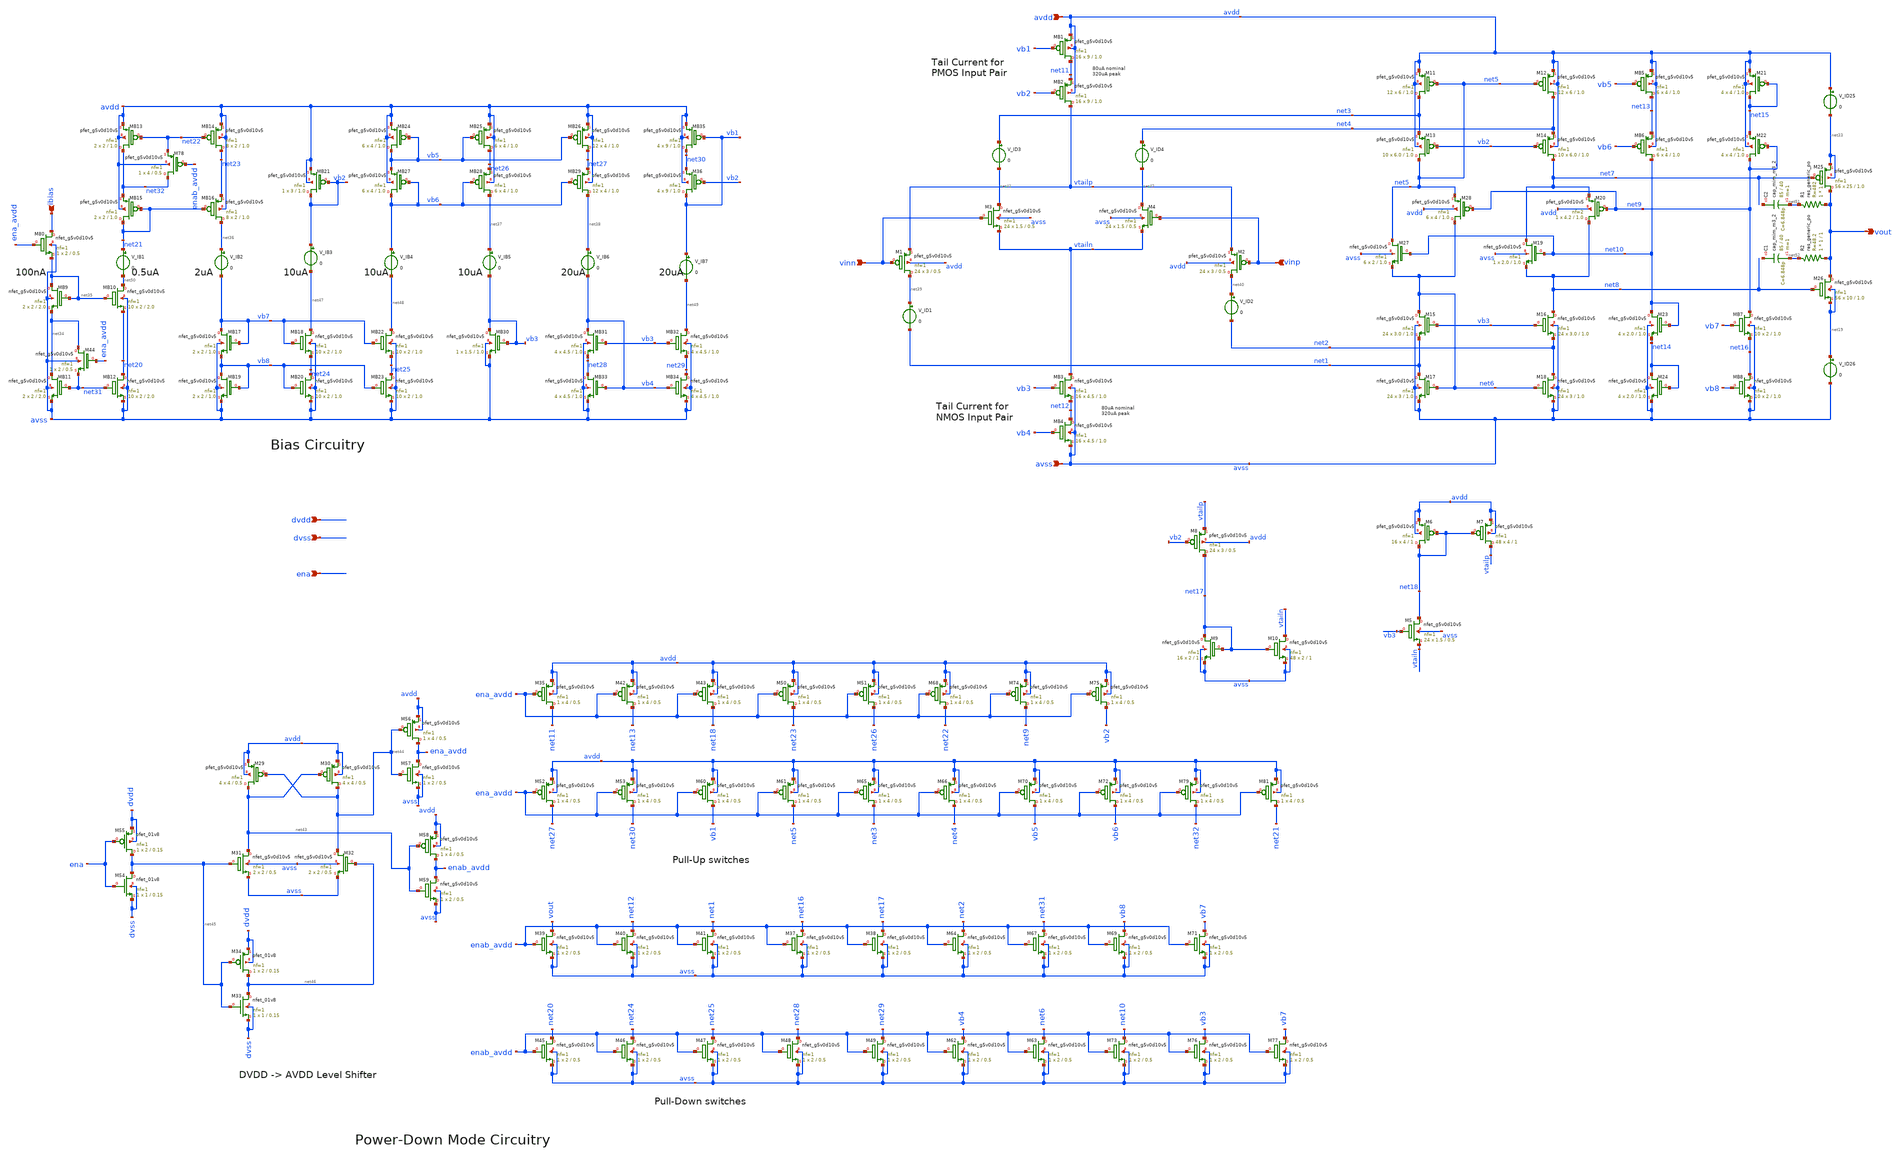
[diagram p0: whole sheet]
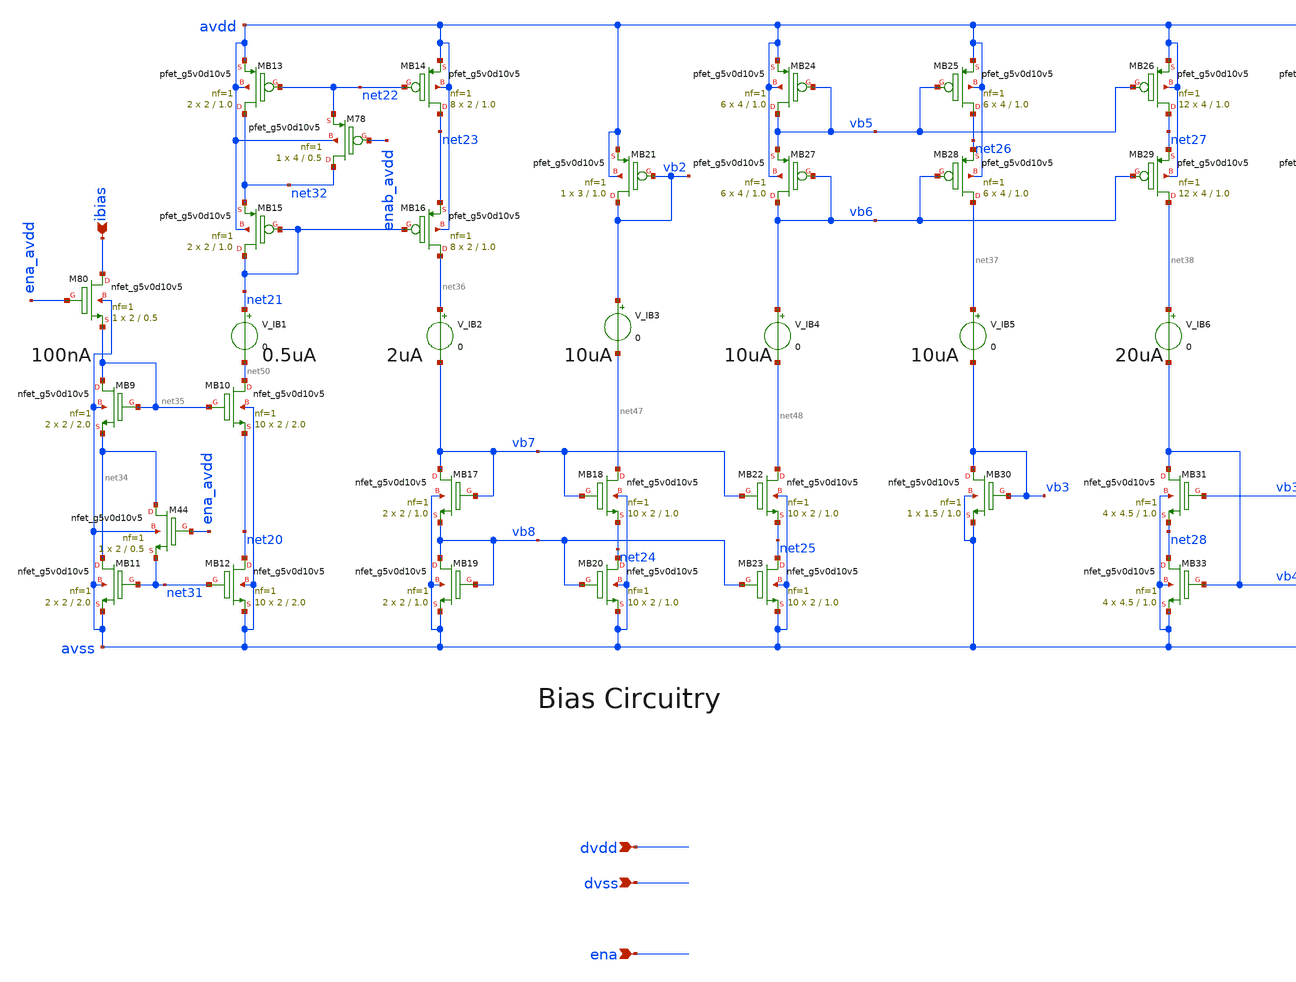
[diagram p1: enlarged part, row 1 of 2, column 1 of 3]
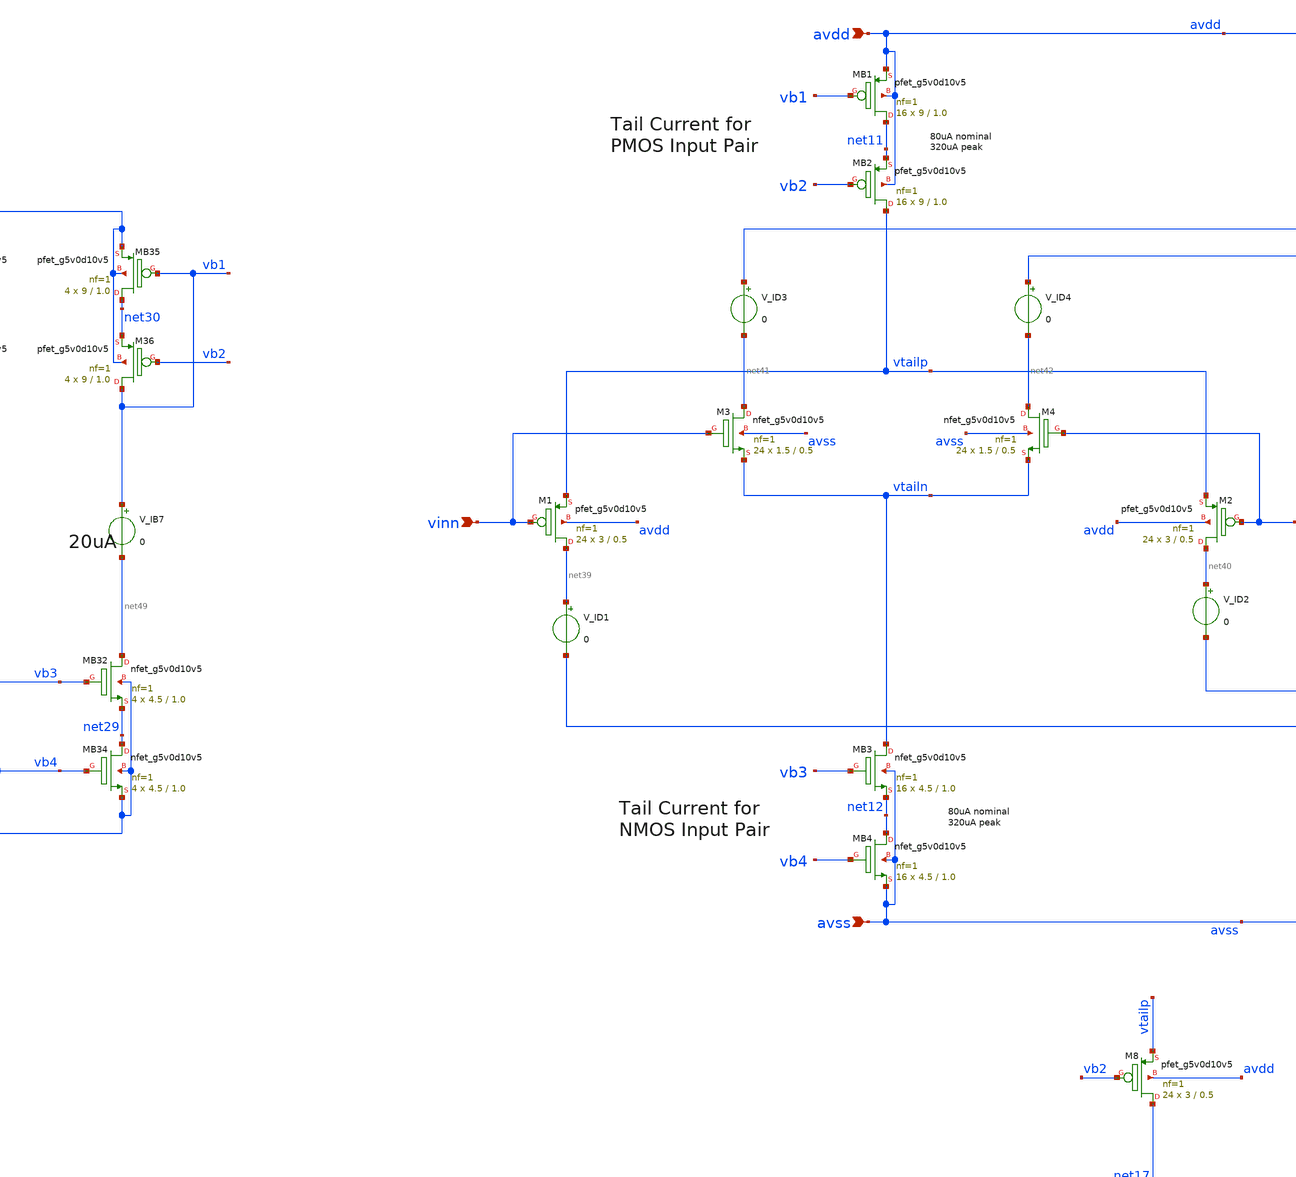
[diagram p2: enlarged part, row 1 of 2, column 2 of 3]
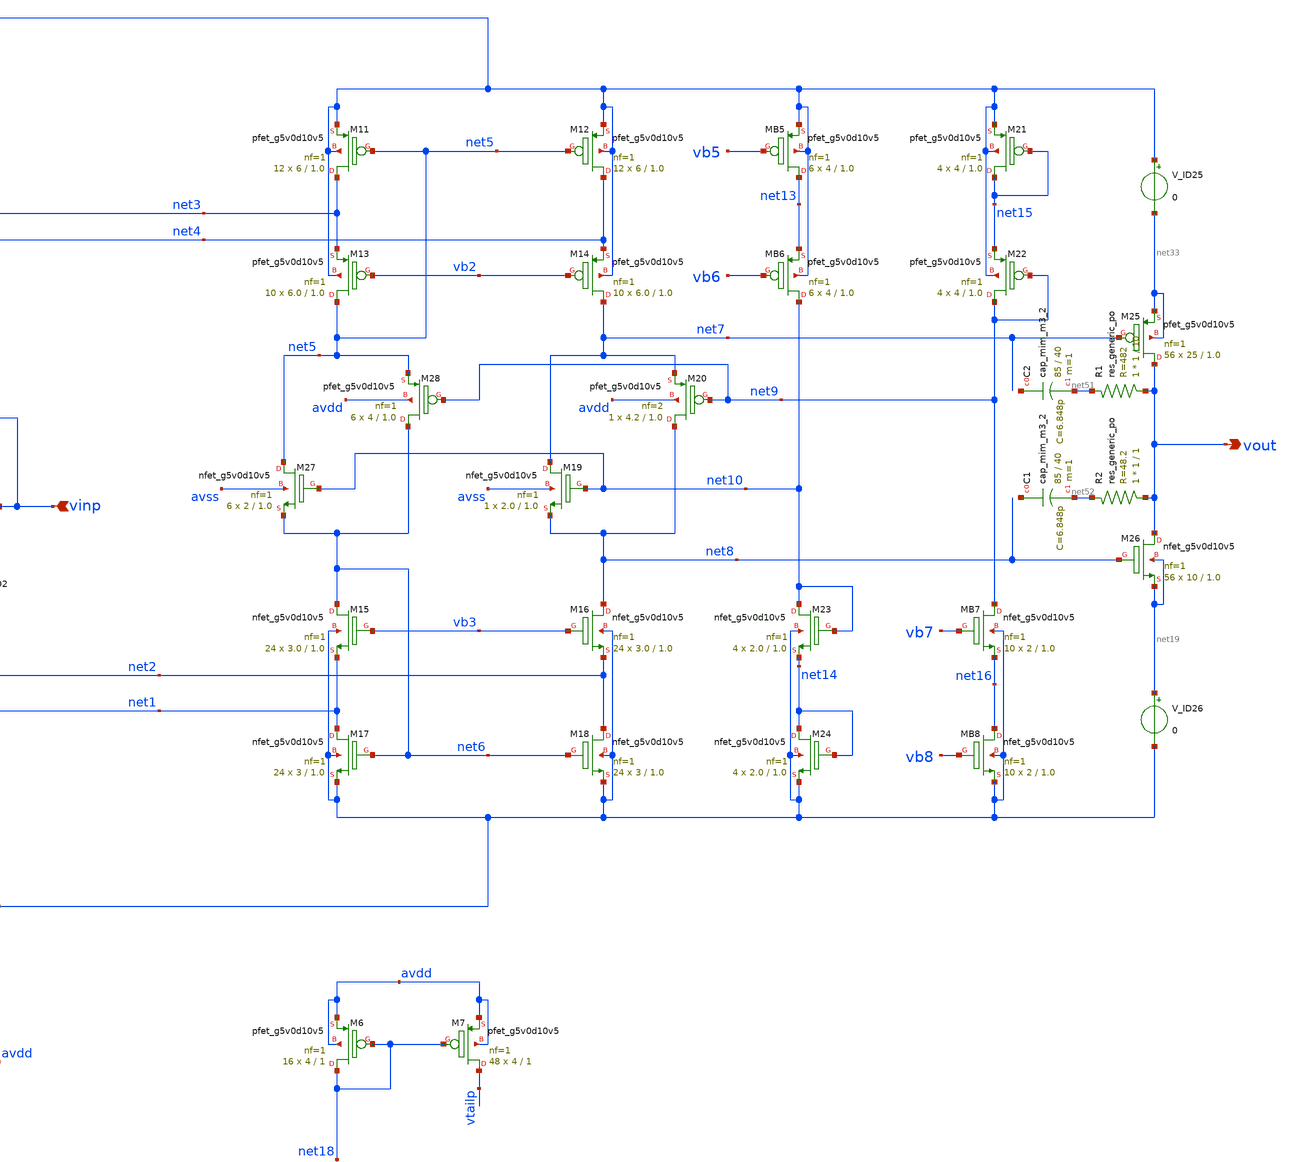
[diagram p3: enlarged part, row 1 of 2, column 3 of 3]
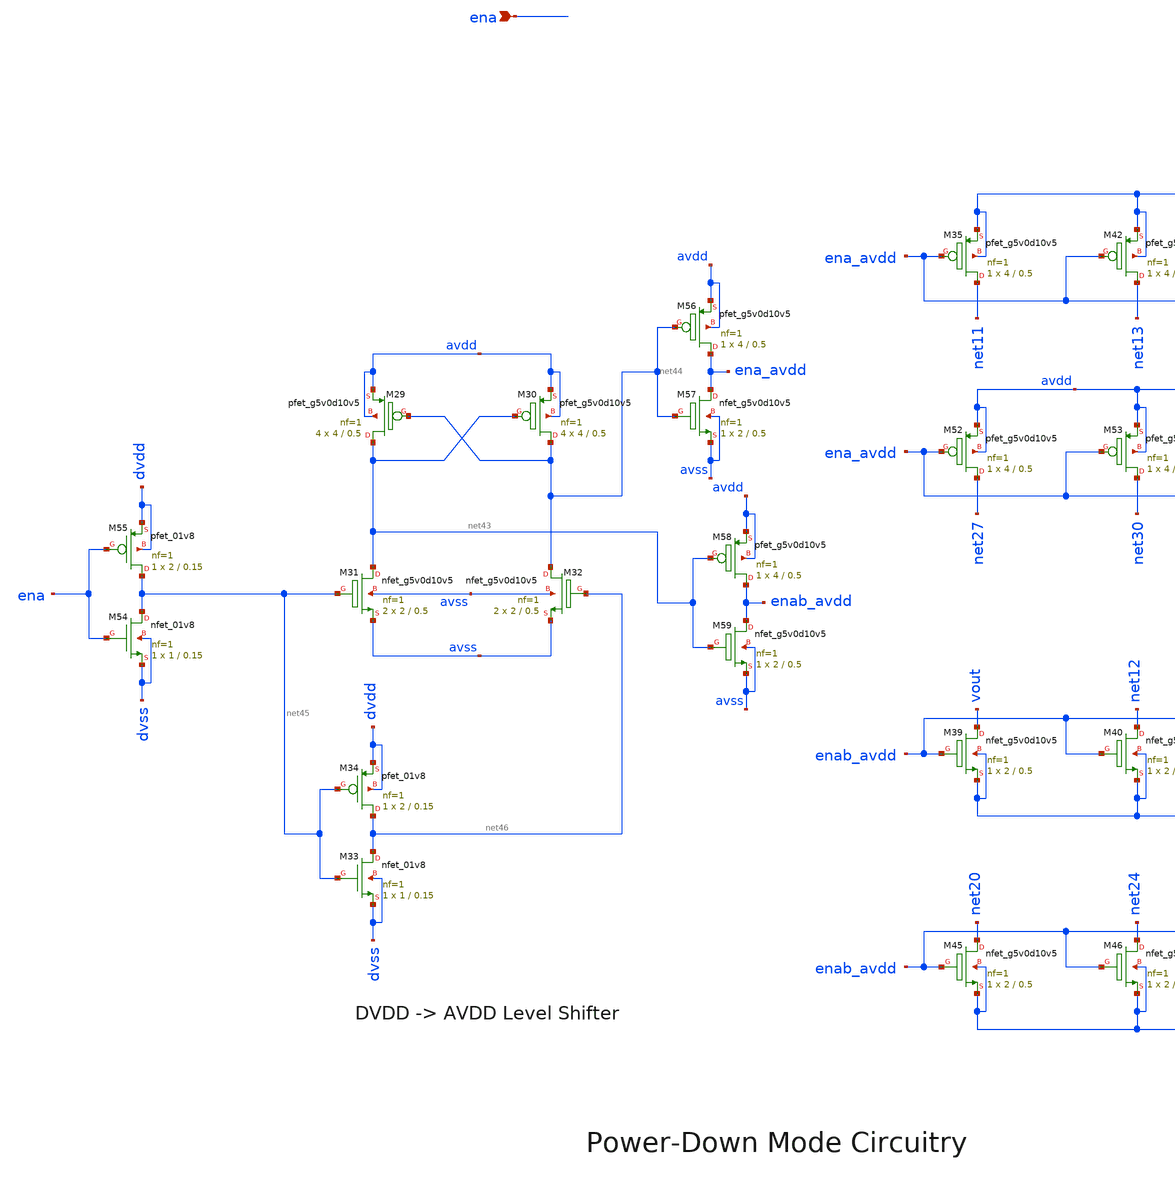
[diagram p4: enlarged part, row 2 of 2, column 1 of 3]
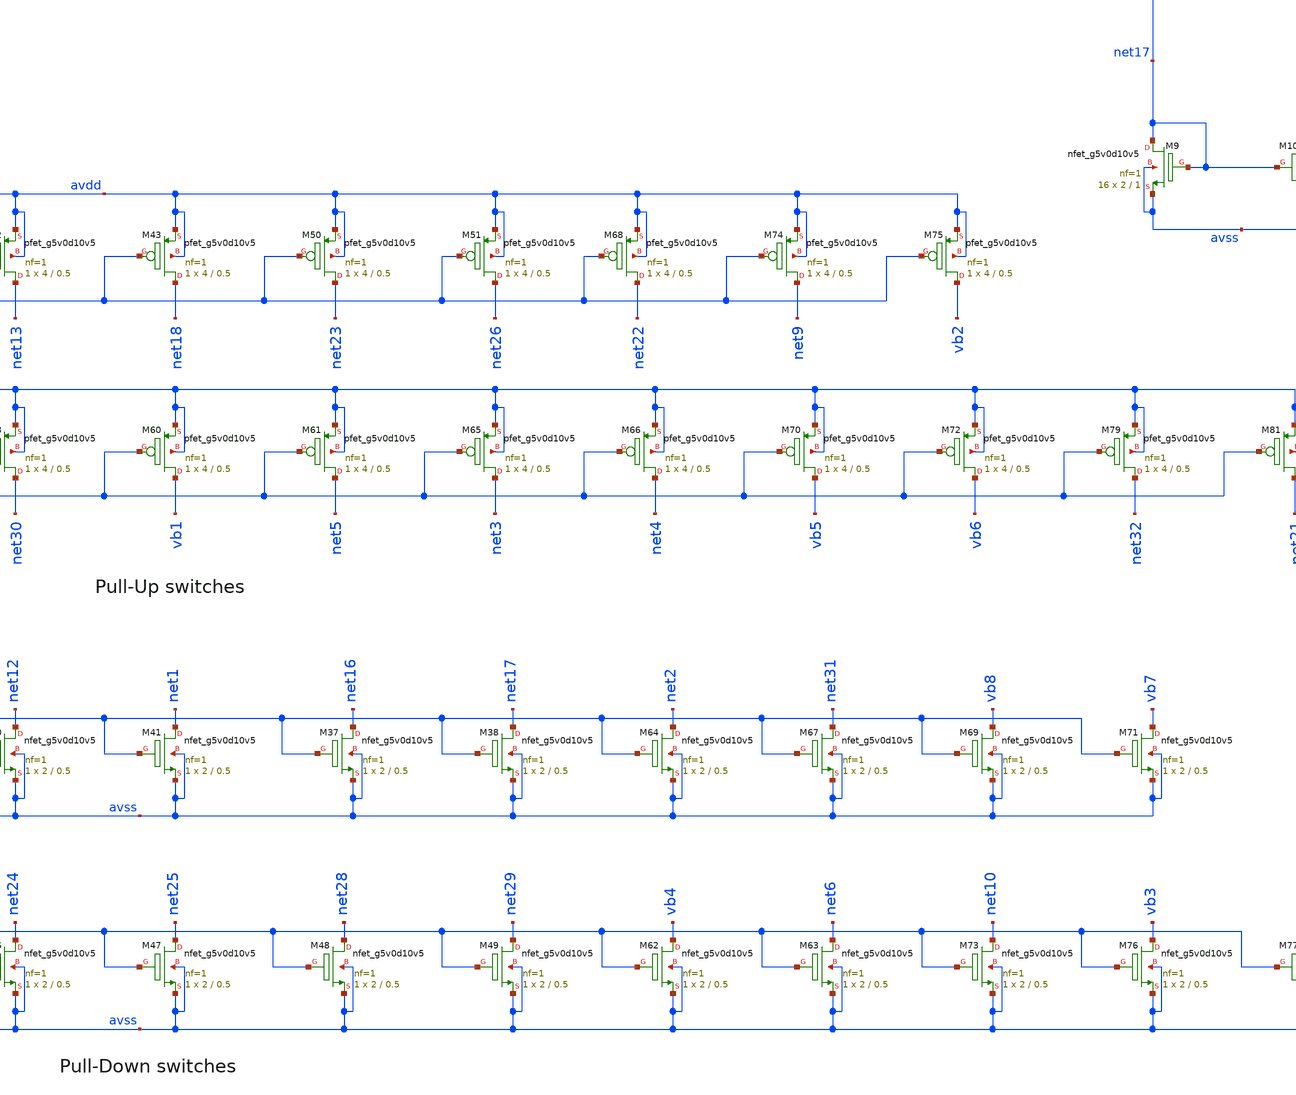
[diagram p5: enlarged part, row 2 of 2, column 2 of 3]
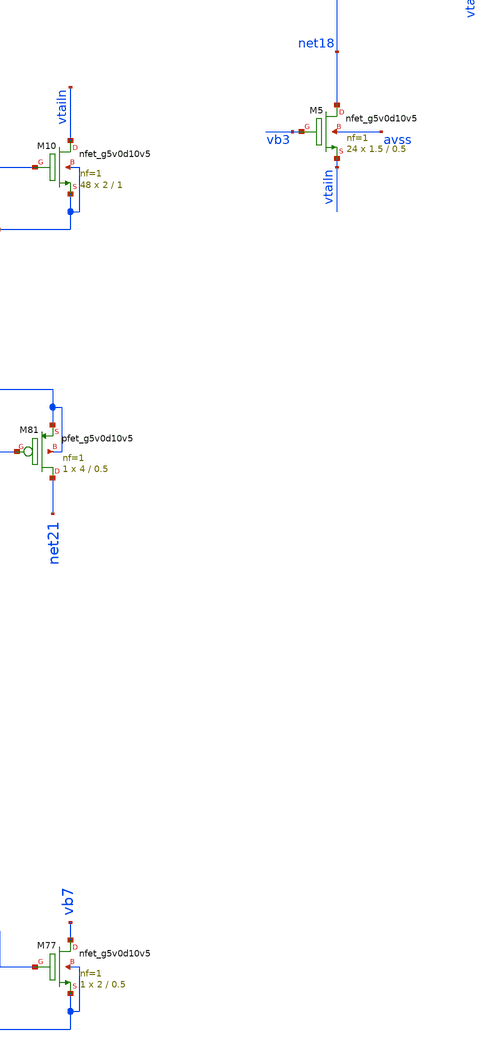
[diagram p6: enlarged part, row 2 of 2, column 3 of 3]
** sch_path: xschem/sky130_td_ip__opamp_hp.sch
**.subckt sky130_td_ip__opamp_hp vinn vinp vout ena ibias avss avdd dvdd dvss
*.ipin vinn
*.ipin vinp
*.opin vout
*.ipin ena
*.ipin ibias
*.ipin avss
*.ipin avdd
*.ipin dvdd
*.ipin dvss
XM3 net41 vinn vtailn avss sky130_fd_pr__nfet_g5v0d10v5 L=0.5 W=1.5 nf=1 ad='int((nf+1)/2) * W/nf * 0.29'
+ as='int((nf+2)/2) * W/nf * 0.29' pd='2*int((nf+1)/2) * (W/nf + 0.29)' ps='2*int((nf+2)/2) * (W/nf + 0.29)'
+ nrd='0.29 / W' nrs='0.29 / W' sa=0 sb=0 sd=0 mult=24 m=24
XM4 net42 vinp vtailn avss sky130_fd_pr__nfet_g5v0d10v5 L=0.5 W=1.5 nf=1 ad='int((nf+1)/2) * W/nf * 0.29'
+ as='int((nf+2)/2) * W/nf * 0.29' pd='2*int((nf+1)/2) * (W/nf + 0.29)' ps='2*int((nf+2)/2) * (W/nf + 0.29)'
+ nrd='0.29 / W' nrs='0.29 / W' sa=0 sb=0 sd=0 mult=24 m=24
XMB3 vtailn vb3 net12 avss sky130_fd_pr__nfet_g5v0d10v5 L=1.0 W=4.5 nf=1 ad='int((nf+1)/2) * W/nf * 0.29'
+ as='int((nf+2)/2) * W/nf * 0.29' pd='2*int((nf+1)/2) * (W/nf + 0.29)' ps='2*int((nf+2)/2) * (W/nf + 0.29)'
+ nrd='0.29 / W' nrs='0.29 / W' sa=0 sb=0 sd=0 mult=16 m=16
XMB4 net12 vb4 avss avss sky130_fd_pr__nfet_g5v0d10v5 L=1.0 W=4.5 nf=1 ad='int((nf+1)/2) * W/nf * 0.29'
+ as='int((nf+2)/2) * W/nf * 0.29' pd='2*int((nf+1)/2) * (W/nf + 0.29)' ps='2*int((nf+2)/2) * (W/nf + 0.29)'
+ nrd='0.29 / W' nrs='0.29 / W' sa=0 sb=0 sd=0 mult=16 m=16
XM1 net39 vinn vtailp avdd sky130_fd_pr__pfet_g5v0d10v5 L=0.5 W=3 nf=1 ad='int((nf+1)/2) * W/nf * 0.29'
+ as='int((nf+2)/2) * W/nf * 0.29' pd='2*int((nf+1)/2) * (W/nf + 0.29)' ps='2*int((nf+2)/2) * (W/nf + 0.29)'
+ nrd='0.29 / W' nrs='0.29 / W' sa=0 sb=0 sd=0 mult=24 m=24
XM2 net40 vinp vtailp avdd sky130_fd_pr__pfet_g5v0d10v5 L=0.5 W=3 nf=1 ad='int((nf+1)/2) * W/nf * 0.29'
+ as='int((nf+2)/2) * W/nf * 0.29' pd='2*int((nf+1)/2) * (W/nf + 0.29)' ps='2*int((nf+2)/2) * (W/nf + 0.29)'
+ nrd='0.29 / W' nrs='0.29 / W' sa=0 sb=0 sd=0 mult=24 m=24
XMB2 vtailp vb2 net11 avdd sky130_fd_pr__pfet_g5v0d10v5 L=1.0 W=9 nf=1 ad='int((nf+1)/2) * W/nf * 0.29'
+ as='int((nf+2)/2) * W/nf * 0.29' pd='2*int((nf+1)/2) * (W/nf + 0.29)' ps='2*int((nf+2)/2) * (W/nf + 0.29)'
+ nrd='0.29 / W' nrs='0.29 / W' sa=0 sb=0 sd=0 mult=16 m=16
XMB1 net11 vb1 avdd avdd sky130_fd_pr__pfet_g5v0d10v5 L=1.0 W=9 nf=1 ad='int((nf+1)/2) * W/nf * 0.29'
+ as='int((nf+2)/2) * W/nf * 0.29' pd='2*int((nf+1)/2) * (W/nf + 0.29)' ps='2*int((nf+2)/2) * (W/nf + 0.29)'
+ nrd='0.29 / W' nrs='0.29 / W' sa=0 sb=0 sd=0 mult=16 m=16
XM12 net4 net5 avdd avdd sky130_fd_pr__pfet_g5v0d10v5 L=1.0 W=6 nf=1 ad='int((nf+1)/2) * W/nf * 0.29'
+ as='int((nf+2)/2) * W/nf * 0.29' pd='2*int((nf+1)/2) * (W/nf + 0.29)' ps='2*int((nf+2)/2) * (W/nf + 0.29)'
+ nrd='0.29 / W' nrs='0.29 / W' sa=0 sb=0 sd=0 mult=12 m=12
XM11 net3 net5 avdd avdd sky130_fd_pr__pfet_g5v0d10v5 L=1.0 W=6 nf=1 ad='int((nf+1)/2) * W/nf * 0.29'
+ as='int((nf+2)/2) * W/nf * 0.29' pd='2*int((nf+1)/2) * (W/nf + 0.29)' ps='2*int((nf+2)/2) * (W/nf + 0.29)'
+ nrd='0.29 / W' nrs='0.29 / W' sa=0 sb=0 sd=0 mult=12 m=12
XM14 net7 vb2 net4 avdd sky130_fd_pr__pfet_g5v0d10v5 L=1.0 W=6.0 nf=1 ad='int((nf+1)/2) * W/nf * 0.29'
+ as='int((nf+2)/2) * W/nf * 0.29' pd='2*int((nf+1)/2) * (W/nf + 0.29)' ps='2*int((nf+2)/2) * (W/nf + 0.29)'
+ nrd='0.29 / W' nrs='0.29 / W' sa=0 sb=0 sd=0 mult=10 m=10
XM13 net5 vb2 net3 avdd sky130_fd_pr__pfet_g5v0d10v5 L=1.0 W=6.0 nf=1 ad='int((nf+1)/2) * W/nf * 0.29'
+ as='int((nf+2)/2) * W/nf * 0.29' pd='2*int((nf+1)/2) * (W/nf + 0.29)' ps='2*int((nf+2)/2) * (W/nf + 0.29)'
+ nrd='0.29 / W' nrs='0.29 / W' sa=0 sb=0 sd=0 mult=10 m=10
XM18 net2 net6 avss avss sky130_fd_pr__nfet_g5v0d10v5 L=1.0 W=3 nf=1 ad='int((nf+1)/2) * W/nf * 0.29'
+ as='int((nf+2)/2) * W/nf * 0.29' pd='2*int((nf+1)/2) * (W/nf + 0.29)' ps='2*int((nf+2)/2) * (W/nf + 0.29)'
+ nrd='0.29 / W' nrs='0.29 / W' sa=0 sb=0 sd=0 mult=24 m=24
XM16 net8 vb3 net2 avss sky130_fd_pr__nfet_g5v0d10v5 L=1.0 W=3.0 nf=1 ad='int((nf+1)/2) * W/nf * 0.29'
+ as='int((nf+2)/2) * W/nf * 0.29' pd='2*int((nf+1)/2) * (W/nf + 0.29)' ps='2*int((nf+2)/2) * (W/nf + 0.29)'
+ nrd='0.29 / W' nrs='0.29 / W' sa=0 sb=0 sd=0 mult=24 m=24
XM17 net1 net6 avss avss sky130_fd_pr__nfet_g5v0d10v5 L=1.0 W=3 nf=1 ad='int((nf+1)/2) * W/nf * 0.29'
+ as='int((nf+2)/2) * W/nf * 0.29' pd='2*int((nf+1)/2) * (W/nf + 0.29)' ps='2*int((nf+2)/2) * (W/nf + 0.29)'
+ nrd='0.29 / W' nrs='0.29 / W' sa=0 sb=0 sd=0 mult=24 m=24
XM15 net6 vb3 net1 avss sky130_fd_pr__nfet_g5v0d10v5 L=1.0 W=3.0 nf=1 ad='int((nf+1)/2) * W/nf * 0.29'
+ as='int((nf+2)/2) * W/nf * 0.29' pd='2*int((nf+1)/2) * (W/nf + 0.29)' ps='2*int((nf+2)/2) * (W/nf + 0.29)'
+ nrd='0.29 / W' nrs='0.29 / W' sa=0 sb=0 sd=0 mult=24 m=24
XM28 net6 net9 net5 avdd sky130_fd_pr__pfet_g5v0d10v5 L=1.0 W=4 nf=1 ad='int((nf+1)/2) * W/nf * 0.29'
+ as='int((nf+2)/2) * W/nf * 0.29' pd='2*int((nf+1)/2) * (W/nf + 0.29)' ps='2*int((nf+2)/2) * (W/nf + 0.29)'
+ nrd='0.29 / W' nrs='0.29 / W' sa=0 sb=0 sd=0 mult=6 m=6
XM27 net5 net10 net6 avss sky130_fd_pr__nfet_g5v0d10v5 L=1.0 W=2 nf=1 ad='int((nf+1)/2) * W/nf * 0.29'
+ as='int((nf+2)/2) * W/nf * 0.29' pd='2*int((nf+1)/2) * (W/nf + 0.29)' ps='2*int((nf+2)/2) * (W/nf + 0.29)'
+ nrd='0.29 / W' nrs='0.29 / W' sa=0 sb=0 sd=0 mult=6 m=6
XM20 net8 net9 net7 avdd sky130_fd_pr__pfet_g5v0d10v5 L=1.0 W=4.2 nf=2 ad='int((nf+1)/2) * W/nf * 0.29'
+ as='int((nf+2)/2) * W/nf * 0.29' pd='2*int((nf+1)/2) * (W/nf + 0.29)' ps='2*int((nf+2)/2) * (W/nf + 0.29)'
+ nrd='0.29 / W' nrs='0.29 / W' sa=0 sb=0 sd=0 mult=1 m=1
XM19 net7 net10 net8 avss sky130_fd_pr__nfet_g5v0d10v5 L=1.0 W=2.0 nf=1 ad='int((nf+1)/2) * W/nf * 0.29'
+ as='int((nf+2)/2) * W/nf * 0.29' pd='2*int((nf+1)/2) * (W/nf + 0.29)' ps='2*int((nf+2)/2) * (W/nf + 0.29)'
+ nrd='0.29 / W' nrs='0.29 / W' sa=0 sb=0 sd=0 mult=1 m=1
XM26 vout net8 net19 net19 sky130_fd_pr__nfet_g5v0d10v5 L=1.0 W=10 nf=1 ad='int((nf+1)/2) * W/nf * 0.29'
+ as='int((nf+2)/2) * W/nf * 0.29' pd='2*int((nf+1)/2) * (W/nf + 0.29)' ps='2*int((nf+2)/2) * (W/nf + 0.29)'
+ nrd='0.29 / W' nrs='0.29 / W' sa=0 sb=0 sd=0 mult=56 m=56
XM25 vout net7 net33 net33 sky130_fd_pr__pfet_g5v0d10v5 L=1.0 W=25 nf=1 ad='int((nf+1)/2) * W/nf * 0.29'
+ as='int((nf+2)/2) * W/nf * 0.29' pd='2*int((nf+1)/2) * (W/nf + 0.29)' ps='2*int((nf+2)/2) * (W/nf + 0.29)'
+ nrd='0.29 / W' nrs='0.29 / W' sa=0 sb=0 sd=0 mult=56 m=56
XMB9 net35 net35 net34 avss sky130_fd_pr__nfet_g5v0d10v5 L=2.0 W=2 nf=1 ad='int((nf+1)/2) * W/nf * 0.29'
+ as='int((nf+2)/2) * W/nf * 0.29' pd='2*int((nf+1)/2) * (W/nf + 0.29)' ps='2*int((nf+2)/2) * (W/nf + 0.29)'
+ nrd='0.29 / W' nrs='0.29 / W' sa=0 sb=0 sd=0 mult=2 m=2
XMB11 net34 net31 avss avss sky130_fd_pr__nfet_g5v0d10v5 L=2.0 W=2 nf=1 ad='int((nf+1)/2) * W/nf * 0.29'
+ as='int((nf+2)/2) * W/nf * 0.29' pd='2*int((nf+1)/2) * (W/nf + 0.29)' ps='2*int((nf+2)/2) * (W/nf + 0.29)'
+ nrd='0.29 / W' nrs='0.29 / W' sa=0 sb=0 sd=0 mult=2 m=2
XMB10 net50 net35 net20 avss sky130_fd_pr__nfet_g5v0d10v5 L=2.0 W=2 nf=1 ad='int((nf+1)/2) * W/nf * 0.29'
+ as='int((nf+2)/2) * W/nf * 0.29' pd='2*int((nf+1)/2) * (W/nf + 0.29)' ps='2*int((nf+2)/2) * (W/nf + 0.29)'
+ nrd='0.29 / W' nrs='0.29 / W' sa=0 sb=0 sd=0 mult=10 m=10
XMB12 net20 net31 avss avss sky130_fd_pr__nfet_g5v0d10v5 L=2.0 W=2 nf=1 ad='int((nf+1)/2) * W/nf * 0.29'
+ as='int((nf+2)/2) * W/nf * 0.29' pd='2*int((nf+1)/2) * (W/nf + 0.29)' ps='2*int((nf+2)/2) * (W/nf + 0.29)'
+ nrd='0.29 / W' nrs='0.29 / W' sa=0 sb=0 sd=0 mult=10 m=10
XMB15 net21 net21 net32 avdd sky130_fd_pr__pfet_g5v0d10v5 L=1.0 W=2 nf=1 ad='int((nf+1)/2) * W/nf * 0.29'
+ as='int((nf+2)/2) * W/nf * 0.29' pd='2*int((nf+1)/2) * (W/nf + 0.29)' ps='2*int((nf+2)/2) * (W/nf + 0.29)'
+ nrd='0.29 / W' nrs='0.29 / W' sa=0 sb=0 sd=0 mult=2 m=2
XMB13 net32 net22 avdd avdd sky130_fd_pr__pfet_g5v0d10v5 L=1.0 W=2 nf=1 ad='int((nf+1)/2) * W/nf * 0.29'
+ as='int((nf+2)/2) * W/nf * 0.29' pd='2*int((nf+1)/2) * (W/nf + 0.29)' ps='2*int((nf+2)/2) * (W/nf + 0.29)'
+ nrd='0.29 / W' nrs='0.29 / W' sa=0 sb=0 sd=0 mult=2 m=2
XMB16 net36 net21 net23 avdd sky130_fd_pr__pfet_g5v0d10v5 L=1.0 W=2 nf=1 ad='int((nf+1)/2) * W/nf * 0.29'
+ as='int((nf+2)/2) * W/nf * 0.29' pd='2*int((nf+1)/2) * (W/nf + 0.29)' ps='2*int((nf+2)/2) * (W/nf + 0.29)'
+ nrd='0.29 / W' nrs='0.29 / W' sa=0 sb=0 sd=0 mult=8 m=8
XMB14 net23 net22 avdd avdd sky130_fd_pr__pfet_g5v0d10v5 L=1.0 W=2 nf=1 ad='int((nf+1)/2) * W/nf * 0.29'
+ as='int((nf+2)/2) * W/nf * 0.29' pd='2*int((nf+1)/2) * (W/nf + 0.29)' ps='2*int((nf+2)/2) * (W/nf + 0.29)'
+ nrd='0.29 / W' nrs='0.29 / W' sa=0 sb=0 sd=0 mult=8 m=8
XMB17 vb7 vb7 vb8 avss sky130_fd_pr__nfet_g5v0d10v5 L=1.0 W=2 nf=1 ad='int((nf+1)/2) * W/nf * 0.29' as='int((nf+2)/2) * W/nf * 0.29'
+ pd='2*int((nf+1)/2) * (W/nf + 0.29)' ps='2*int((nf+2)/2) * (W/nf + 0.29)' nrd='0.29 / W' nrs='0.29 / W'
+ sa=0 sb=0 sd=0 mult=2 m=2
XMB19 vb8 vb8 avss avss sky130_fd_pr__nfet_g5v0d10v5 L=1.0 W=2 nf=1 ad='int((nf+1)/2) * W/nf * 0.29'
+ as='int((nf+2)/2) * W/nf * 0.29' pd='2*int((nf+1)/2) * (W/nf + 0.29)' ps='2*int((nf+2)/2) * (W/nf + 0.29)'
+ nrd='0.29 / W' nrs='0.29 / W' sa=0 sb=0 sd=0 mult=2 m=2
XMB18 net47 vb7 net24 avss sky130_fd_pr__nfet_g5v0d10v5 L=1.0 W=2 nf=1 ad='int((nf+1)/2) * W/nf * 0.29'
+ as='int((nf+2)/2) * W/nf * 0.29' pd='2*int((nf+1)/2) * (W/nf + 0.29)' ps='2*int((nf+2)/2) * (W/nf + 0.29)'
+ nrd='0.29 / W' nrs='0.29 / W' sa=0 sb=0 sd=0 mult=10 m=10
XMB20 net24 vb8 avss avss sky130_fd_pr__nfet_g5v0d10v5 L=1.0 W=2 nf=1 ad='int((nf+1)/2) * W/nf * 0.29'
+ as='int((nf+2)/2) * W/nf * 0.29' pd='2*int((nf+1)/2) * (W/nf + 0.29)' ps='2*int((nf+2)/2) * (W/nf + 0.29)'
+ nrd='0.29 / W' nrs='0.29 / W' sa=0 sb=0 sd=0 mult=10 m=10
XMB22 net48 vb7 net25 avss sky130_fd_pr__nfet_g5v0d10v5 L=1.0 W=2 nf=1 ad='int((nf+1)/2) * W/nf * 0.29'
+ as='int((nf+2)/2) * W/nf * 0.29' pd='2*int((nf+1)/2) * (W/nf + 0.29)' ps='2*int((nf+2)/2) * (W/nf + 0.29)'
+ nrd='0.29 / W' nrs='0.29 / W' sa=0 sb=0 sd=0 mult=10 m=10
XMB23 net25 vb8 avss avss sky130_fd_pr__nfet_g5v0d10v5 L=1.0 W=2 nf=1 ad='int((nf+1)/2) * W/nf * 0.29'
+ as='int((nf+2)/2) * W/nf * 0.29' pd='2*int((nf+1)/2) * (W/nf + 0.29)' ps='2*int((nf+2)/2) * (W/nf + 0.29)'
+ nrd='0.29 / W' nrs='0.29 / W' sa=0 sb=0 sd=0 mult=10 m=10
XMB21 vb2 vb2 avdd avdd sky130_fd_pr__pfet_g5v0d10v5 L=1.0 W=3 nf=1 ad='int((nf+1)/2) * W/nf * 0.29'
+ as='int((nf+2)/2) * W/nf * 0.29' pd='2*int((nf+1)/2) * (W/nf + 0.29)' ps='2*int((nf+2)/2) * (W/nf + 0.29)'
+ nrd='0.29 / W' nrs='0.29 / W' sa=0 sb=0 sd=0 mult=1 m=1
XMB27 vb6 vb6 vb5 avdd sky130_fd_pr__pfet_g5v0d10v5 L=1.0 W=4 nf=1 ad='int((nf+1)/2) * W/nf * 0.29' as='int((nf+2)/2) * W/nf * 0.29'
+ pd='2*int((nf+1)/2) * (W/nf + 0.29)' ps='2*int((nf+2)/2) * (W/nf + 0.29)' nrd='0.29 / W' nrs='0.29 / W'
+ sa=0 sb=0 sd=0 mult=6 m=6
XMB24 vb5 vb5 avdd avdd sky130_fd_pr__pfet_g5v0d10v5 L=1.0 W=4 nf=1 ad='int((nf+1)/2) * W/nf * 0.29'
+ as='int((nf+2)/2) * W/nf * 0.29' pd='2*int((nf+1)/2) * (W/nf + 0.29)' ps='2*int((nf+2)/2) * (W/nf + 0.29)'
+ nrd='0.29 / W' nrs='0.29 / W' sa=0 sb=0 sd=0 mult=6 m=6
XMB28 net37 vb6 net26 avdd sky130_fd_pr__pfet_g5v0d10v5 L=1.0 W=4 nf=1 ad='int((nf+1)/2) * W/nf * 0.29'
+ as='int((nf+2)/2) * W/nf * 0.29' pd='2*int((nf+1)/2) * (W/nf + 0.29)' ps='2*int((nf+2)/2) * (W/nf + 0.29)'
+ nrd='0.29 / W' nrs='0.29 / W' sa=0 sb=0 sd=0 mult=6 m=6
XMB25 net26 vb5 avdd avdd sky130_fd_pr__pfet_g5v0d10v5 L=1.0 W=4 nf=1 ad='int((nf+1)/2) * W/nf * 0.29'
+ as='int((nf+2)/2) * W/nf * 0.29' pd='2*int((nf+1)/2) * (W/nf + 0.29)' ps='2*int((nf+2)/2) * (W/nf + 0.29)'
+ nrd='0.29 / W' nrs='0.29 / W' sa=0 sb=0 sd=0 mult=6 m=6
XMB29 net38 vb6 net27 avdd sky130_fd_pr__pfet_g5v0d10v5 L=1.0 W=4 nf=1 ad='int((nf+1)/2) * W/nf * 0.29'
+ as='int((nf+2)/2) * W/nf * 0.29' pd='2*int((nf+1)/2) * (W/nf + 0.29)' ps='2*int((nf+2)/2) * (W/nf + 0.29)'
+ nrd='0.29 / W' nrs='0.29 / W' sa=0 sb=0 sd=0 mult=12 m=12
XMB26 net27 vb5 avdd avdd sky130_fd_pr__pfet_g5v0d10v5 L=1.0 W=4 nf=1 ad='int((nf+1)/2) * W/nf * 0.29'
+ as='int((nf+2)/2) * W/nf * 0.29' pd='2*int((nf+1)/2) * (W/nf + 0.29)' ps='2*int((nf+2)/2) * (W/nf + 0.29)'
+ nrd='0.29 / W' nrs='0.29 / W' sa=0 sb=0 sd=0 mult=12 m=12
XMB30 vb3 vb3 avss avss sky130_fd_pr__nfet_g5v0d10v5 L=1.0 W=1.5 nf=1 ad='int((nf+1)/2) * W/nf * 0.29'
+ as='int((nf+2)/2) * W/nf * 0.29' pd='2*int((nf+1)/2) * (W/nf + 0.29)' ps='2*int((nf+2)/2) * (W/nf + 0.29)'
+ nrd='0.29 / W' nrs='0.29 / W' sa=0 sb=0 sd=0 mult=1 m=1
XMB31 vb4 vb3 net28 avss sky130_fd_pr__nfet_g5v0d10v5 L=1.0 W=4.5 nf=1 ad='int((nf+1)/2) * W/nf * 0.29'
+ as='int((nf+2)/2) * W/nf * 0.29' pd='2*int((nf+1)/2) * (W/nf + 0.29)' ps='2*int((nf+2)/2) * (W/nf + 0.29)'
+ nrd='0.29 / W' nrs='0.29 / W' sa=0 sb=0 sd=0 mult=4 m=4
XMB33 net28 vb4 avss avss sky130_fd_pr__nfet_g5v0d10v5 L=1.0 W=4.5 nf=1 ad='int((nf+1)/2) * W/nf * 0.29'
+ as='int((nf+2)/2) * W/nf * 0.29' pd='2*int((nf+1)/2) * (W/nf + 0.29)' ps='2*int((nf+2)/2) * (W/nf + 0.29)'
+ nrd='0.29 / W' nrs='0.29 / W' sa=0 sb=0 sd=0 mult=4 m=4
XMB32 net49 vb3 net29 avss sky130_fd_pr__nfet_g5v0d10v5 L=1.0 W=4.5 nf=1 ad='int((nf+1)/2) * W/nf * 0.29'
+ as='int((nf+2)/2) * W/nf * 0.29' pd='2*int((nf+1)/2) * (W/nf + 0.29)' ps='2*int((nf+2)/2) * (W/nf + 0.29)'
+ nrd='0.29 / W' nrs='0.29 / W' sa=0 sb=0 sd=0 mult=4 m=4
XMB34 net29 vb4 avss avss sky130_fd_pr__nfet_g5v0d10v5 L=1.0 W=4.5 nf=1 ad='int((nf+1)/2) * W/nf * 0.29'
+ as='int((nf+2)/2) * W/nf * 0.29' pd='2*int((nf+1)/2) * (W/nf + 0.29)' ps='2*int((nf+2)/2) * (W/nf + 0.29)'
+ nrd='0.29 / W' nrs='0.29 / W' sa=0 sb=0 sd=0 mult=4 m=4
XM36 vb1 vb2 net30 avdd sky130_fd_pr__pfet_g5v0d10v5 L=1.0 W=9 nf=1 ad='int((nf+1)/2) * W/nf * 0.29'
+ as='int((nf+2)/2) * W/nf * 0.29' pd='2*int((nf+1)/2) * (W/nf + 0.29)' ps='2*int((nf+2)/2) * (W/nf + 0.29)'
+ nrd='0.29 / W' nrs='0.29 / W' sa=0 sb=0 sd=0 mult=4 m=4
XMB35 net30 vb1 avdd avdd sky130_fd_pr__pfet_g5v0d10v5 L=1.0 W=9 nf=1 ad='int((nf+1)/2) * W/nf * 0.29'
+ as='int((nf+2)/2) * W/nf * 0.29' pd='2*int((nf+1)/2) * (W/nf + 0.29)' ps='2*int((nf+2)/2) * (W/nf + 0.29)'
+ nrd='0.29 / W' nrs='0.29 / W' sa=0 sb=0 sd=0 mult=4 m=4
XM24 net14 net14 avss avss sky130_fd_pr__nfet_g5v0d10v5 L=1.0 W=2.0 nf=1 ad='int((nf+1)/2) * W/nf * 0.29'
+ as='int((nf+2)/2) * W/nf * 0.29' pd='2*int((nf+1)/2) * (W/nf + 0.29)' ps='2*int((nf+2)/2) * (W/nf + 0.29)'
+ nrd='0.29 / W' nrs='0.29 / W' sa=0 sb=0 sd=0 mult=4 m=4
XM23 net10 net10 net14 avss sky130_fd_pr__nfet_g5v0d10v5 L=1.0 W=2.0 nf=1 ad='int((nf+1)/2) * W/nf * 0.29'
+ as='int((nf+2)/2) * W/nf * 0.29' pd='2*int((nf+1)/2) * (W/nf + 0.29)' ps='2*int((nf+2)/2) * (W/nf + 0.29)'
+ nrd='0.29 / W' nrs='0.29 / W' sa=0 sb=0 sd=0 mult=4 m=4
XMB5 net13 vb5 avdd avdd sky130_fd_pr__pfet_g5v0d10v5 L=1.0 W=4 nf=1 ad='int((nf+1)/2) * W/nf * 0.29'
+ as='int((nf+2)/2) * W/nf * 0.29' pd='2*int((nf+1)/2) * (W/nf + 0.29)' ps='2*int((nf+2)/2) * (W/nf + 0.29)'
+ nrd='0.29 / W' nrs='0.29 / W' sa=0 sb=0 sd=0 mult=6 m=6
XMB6 net10 vb6 net13 avdd sky130_fd_pr__pfet_g5v0d10v5 L=1.0 W=4 nf=1 ad='int((nf+1)/2) * W/nf * 0.29'
+ as='int((nf+2)/2) * W/nf * 0.29' pd='2*int((nf+1)/2) * (W/nf + 0.29)' ps='2*int((nf+2)/2) * (W/nf + 0.29)'
+ nrd='0.29 / W' nrs='0.29 / W' sa=0 sb=0 sd=0 mult=6 m=6
XM21 net15 net15 avdd avdd sky130_fd_pr__pfet_g5v0d10v5 L=1.0 W=4 nf=1 ad='int((nf+1)/2) * W/nf * 0.29'
+ as='int((nf+2)/2) * W/nf * 0.29' pd='2*int((nf+1)/2) * (W/nf + 0.29)' ps='2*int((nf+2)/2) * (W/nf + 0.29)'
+ nrd='0.29 / W' nrs='0.29 / W' sa=0 sb=0 sd=0 mult=4 m=4
XM22 net9 net9 net15 avdd sky130_fd_pr__pfet_g5v0d10v5 L=1.0 W=4 nf=1 ad='int((nf+1)/2) * W/nf * 0.29'
+ as='int((nf+2)/2) * W/nf * 0.29' pd='2*int((nf+1)/2) * (W/nf + 0.29)' ps='2*int((nf+2)/2) * (W/nf + 0.29)'
+ nrd='0.29 / W' nrs='0.29 / W' sa=0 sb=0 sd=0 mult=4 m=4
XMB8 net16 vb8 avss avss sky130_fd_pr__nfet_g5v0d10v5 L=1.0 W=2 nf=1 ad='int((nf+1)/2) * W/nf * 0.29'
+ as='int((nf+2)/2) * W/nf * 0.29' pd='2*int((nf+1)/2) * (W/nf + 0.29)' ps='2*int((nf+2)/2) * (W/nf + 0.29)'
+ nrd='0.29 / W' nrs='0.29 / W' sa=0 sb=0 sd=0 mult=10 m=10
XMB7 net9 vb7 net16 avss sky130_fd_pr__nfet_g5v0d10v5 L=1.0 W=2 nf=1 ad='int((nf+1)/2) * W/nf * 0.29'
+ as='int((nf+2)/2) * W/nf * 0.29' pd='2*int((nf+1)/2) * (W/nf + 0.29)' ps='2*int((nf+2)/2) * (W/nf + 0.29)'
+ nrd='0.29 / W' nrs='0.29 / W' sa=0 sb=0 sd=0 mult=10 m=10
XC1 net53 net52 sky130_fd_pr__cap_mim_m3_2 W=85 L=40 MF=1 m=1
XC2 net54 net51 sky130_fd_pr__cap_mim_m3_2 W=85 L=40 MF=1 m=1
XM5 net18 vb3 vtailn avss sky130_fd_pr__nfet_g5v0d10v5 L=0.5 W=1.5 nf=1 ad='int((nf+1)/2) * W/nf * 0.29'
+ as='int((nf+2)/2) * W/nf * 0.29' pd='2*int((nf+1)/2) * (W/nf + 0.29)' ps='2*int((nf+2)/2) * (W/nf + 0.29)'
+ nrd='0.29 / W' nrs='0.29 / W' sa=0 sb=0 sd=0 mult=24 m=24
XM6 net18 net18 avdd avdd sky130_fd_pr__pfet_g5v0d10v5 L=1 W=4 nf=1 ad='int((nf+1)/2) * W/nf * 0.29'
+ as='int((nf+2)/2) * W/nf * 0.29' pd='2*int((nf+1)/2) * (W/nf + 0.29)' ps='2*int((nf+2)/2) * (W/nf + 0.29)'
+ nrd='0.29 / W' nrs='0.29 / W' sa=0 sb=0 sd=0 mult=16 m=16
XM7 vtailp net18 avdd avdd sky130_fd_pr__pfet_g5v0d10v5 L=1 W=4 nf=1 ad='int((nf+1)/2) * W/nf * 0.29'
+ as='int((nf+2)/2) * W/nf * 0.29' pd='2*int((nf+1)/2) * (W/nf + 0.29)' ps='2*int((nf+2)/2) * (W/nf + 0.29)'
+ nrd='0.29 / W' nrs='0.29 / W' sa=0 sb=0 sd=0 mult=48 m=48
XM8 net17 vb2 vtailp avdd sky130_fd_pr__pfet_g5v0d10v5 L=0.5 W=3 nf=1 ad='int((nf+1)/2) * W/nf * 0.29'
+ as='int((nf+2)/2) * W/nf * 0.29' pd='2*int((nf+1)/2) * (W/nf + 0.29)' ps='2*int((nf+2)/2) * (W/nf + 0.29)'
+ nrd='0.29 / W' nrs='0.29 / W' sa=0 sb=0 sd=0 mult=24 m=24
XM9 net17 net17 avss avss sky130_fd_pr__nfet_g5v0d10v5 L=1 W=2 nf=1 ad='int((nf+1)/2) * W/nf * 0.29'
+ as='int((nf+2)/2) * W/nf * 0.29' pd='2*int((nf+1)/2) * (W/nf + 0.29)' ps='2*int((nf+2)/2) * (W/nf + 0.29)'
+ nrd='0.29 / W' nrs='0.29 / W' sa=0 sb=0 sd=0 mult=16 m=16
XM10 vtailn net17 avss avss sky130_fd_pr__nfet_g5v0d10v5 L=1 W=2 nf=1 ad='int((nf+1)/2) * W/nf * 0.29'
+ as='int((nf+2)/2) * W/nf * 0.29' pd='2*int((nf+1)/2) * (W/nf + 0.29)' ps='2*int((nf+2)/2) * (W/nf + 0.29)'
+ nrd='0.29 / W' nrs='0.29 / W' sa=0 sb=0 sd=0 mult=48 m=48
V_ID1 net39 net1 0
.save i(v_id1)
V_ID2 net40 net2 0
.save i(v_id2)
V_ID3 net3 net41 0
.save i(v_id3)
V_ID4 net4 net42 0
.save i(v_id4)
V_ID25 avdd net33 0
.save i(v_id25)
V_ID26 net19 avss 0
.save i(v_id26)
XM29 net43 net44 avdd avdd sky130_fd_pr__pfet_g5v0d10v5 L=0.5 W=4 nf=1 ad='int((nf+1)/2) * W/nf * 0.29'
+ as='int((nf+2)/2) * W/nf * 0.29' pd='2*int((nf+1)/2) * (W/nf + 0.29)' ps='2*int((nf+2)/2) * (W/nf + 0.29)'
+ nrd='0.29 / W' nrs='0.29 / W' sa=0 sb=0 sd=0 mult=4 m=4
XM30 net44 net43 avdd avdd sky130_fd_pr__pfet_g5v0d10v5 L=0.5 W=4 nf=1 ad='int((nf+1)/2) * W/nf * 0.29'
+ as='int((nf+2)/2) * W/nf * 0.29' pd='2*int((nf+1)/2) * (W/nf + 0.29)' ps='2*int((nf+2)/2) * (W/nf + 0.29)'
+ nrd='0.29 / W' nrs='0.29 / W' sa=0 sb=0 sd=0 mult=4 m=4
XM31 net43 net45 avss avss sky130_fd_pr__nfet_g5v0d10v5 L=0.5 W=2 nf=1 ad='int((nf+1)/2) * W/nf * 0.29'
+ as='int((nf+2)/2) * W/nf * 0.29' pd='2*int((nf+1)/2) * (W/nf + 0.29)' ps='2*int((nf+2)/2) * (W/nf + 0.29)'
+ nrd='0.29 / W' nrs='0.29 / W' sa=0 sb=0 sd=0 mult=2 m=2
XM32 net44 net46 avss avss sky130_fd_pr__nfet_g5v0d10v5 L=0.5 W=2 nf=1 ad='int((nf+1)/2) * W/nf * 0.29'
+ as='int((nf+2)/2) * W/nf * 0.29' pd='2*int((nf+1)/2) * (W/nf + 0.29)' ps='2*int((nf+2)/2) * (W/nf + 0.29)'
+ nrd='0.29 / W' nrs='0.29 / W' sa=0 sb=0 sd=0 mult=2 m=2
XM33 net46 net45 dvss dvss sky130_fd_pr__nfet_01v8 L=0.15 W=1 nf=1 ad='int((nf+1)/2) * W/nf * 0.29' as='int((nf+2)/2) * W/nf * 0.29'
+ pd='2*int((nf+1)/2) * (W/nf + 0.29)' ps='2*int((nf+2)/2) * (W/nf + 0.29)' nrd='0.29 / W' nrs='0.29 / W'
+ sa=0 sb=0 sd=0 mult=1 m=1
XM34 net46 net45 dvdd dvdd sky130_fd_pr__pfet_01v8 L=0.15 W=2 nf=1 ad='int((nf+1)/2) * W/nf * 0.29' as='int((nf+2)/2) * W/nf * 0.29'
+ pd='2*int((nf+1)/2) * (W/nf + 0.29)' ps='2*int((nf+2)/2) * (W/nf + 0.29)' nrd='0.29 / W' nrs='0.29 / W'
+ sa=0 sb=0 sd=0 mult=1 m=1
XM35 net11 ena_avdd avdd avdd sky130_fd_pr__pfet_g5v0d10v5 L=0.5 W=4 nf=1 ad='int((nf+1)/2) * W/nf * 0.29'
+ as='int((nf+2)/2) * W/nf * 0.29' pd='2*int((nf+1)/2) * (W/nf + 0.29)' ps='2*int((nf+2)/2) * (W/nf + 0.29)'
+ nrd='0.29 / W' nrs='0.29 / W' sa=0 sb=0 sd=0 mult=1 m=1
XM39 vout enab_avdd avss avss sky130_fd_pr__nfet_g5v0d10v5 L=0.5 W=2 nf=1 ad='int((nf+1)/2) * W/nf * 0.29'
+ as='int((nf+2)/2) * W/nf * 0.29' pd='2*int((nf+1)/2) * (W/nf + 0.29)' ps='2*int((nf+2)/2) * (W/nf + 0.29)'
+ nrd='0.29 / W' nrs='0.29 / W' sa=0 sb=0 sd=0 mult=1 m=1
XM40 net12 enab_avdd avss avss sky130_fd_pr__nfet_g5v0d10v5 L=0.5 W=2 nf=1 ad='int((nf+1)/2) * W/nf * 0.29'
+ as='int((nf+2)/2) * W/nf * 0.29' pd='2*int((nf+1)/2) * (W/nf + 0.29)' ps='2*int((nf+2)/2) * (W/nf + 0.29)'
+ nrd='0.29 / W' nrs='0.29 / W' sa=0 sb=0 sd=0 mult=1 m=1
XM41 net1 enab_avdd avss avss sky130_fd_pr__nfet_g5v0d10v5 L=0.5 W=2 nf=1 ad='int((nf+1)/2) * W/nf * 0.29'
+ as='int((nf+2)/2) * W/nf * 0.29' pd='2*int((nf+1)/2) * (W/nf + 0.29)' ps='2*int((nf+2)/2) * (W/nf + 0.29)'
+ nrd='0.29 / W' nrs='0.29 / W' sa=0 sb=0 sd=0 mult=1 m=1
XM37 net16 enab_avdd avss avss sky130_fd_pr__nfet_g5v0d10v5 L=0.5 W=2 nf=1 ad='int((nf+1)/2) * W/nf * 0.29'
+ as='int((nf+2)/2) * W/nf * 0.29' pd='2*int((nf+1)/2) * (W/nf + 0.29)' ps='2*int((nf+2)/2) * (W/nf + 0.29)'
+ nrd='0.29 / W' nrs='0.29 / W' sa=0 sb=0 sd=0 mult=1 m=1
XM38 net17 enab_avdd avss avss sky130_fd_pr__nfet_g5v0d10v5 L=0.5 W=2 nf=1 ad='int((nf+1)/2) * W/nf * 0.29'
+ as='int((nf+2)/2) * W/nf * 0.29' pd='2*int((nf+1)/2) * (W/nf + 0.29)' ps='2*int((nf+2)/2) * (W/nf + 0.29)'
+ nrd='0.29 / W' nrs='0.29 / W' sa=0 sb=0 sd=0 mult=1 m=1
XM42 net13 ena_avdd avdd avdd sky130_fd_pr__pfet_g5v0d10v5 L=0.5 W=4 nf=1 ad='int((nf+1)/2) * W/nf * 0.29'
+ as='int((nf+2)/2) * W/nf * 0.29' pd='2*int((nf+1)/2) * (W/nf + 0.29)' ps='2*int((nf+2)/2) * (W/nf + 0.29)'
+ nrd='0.29 / W' nrs='0.29 / W' sa=0 sb=0 sd=0 mult=1 m=1
XM43 net18 ena_avdd avdd avdd sky130_fd_pr__pfet_g5v0d10v5 L=0.5 W=4 nf=1 ad='int((nf+1)/2) * W/nf * 0.29'
+ as='int((nf+2)/2) * W/nf * 0.29' pd='2*int((nf+1)/2) * (W/nf + 0.29)' ps='2*int((nf+2)/2) * (W/nf + 0.29)'
+ nrd='0.29 / W' nrs='0.29 / W' sa=0 sb=0 sd=0 mult=1 m=1
XM44 net34 ena_avdd net31 avss sky130_fd_pr__nfet_g5v0d10v5 L=0.5 W=2 nf=1 ad='int((nf+1)/2) * W/nf * 0.29'
+ as='int((nf+2)/2) * W/nf * 0.29' pd='2*int((nf+1)/2) * (W/nf + 0.29)' ps='2*int((nf+2)/2) * (W/nf + 0.29)'
+ nrd='0.29 / W' nrs='0.29 / W' sa=0 sb=0 sd=0 mult=1 m=1
XM45 net20 enab_avdd avss avss sky130_fd_pr__nfet_g5v0d10v5 L=0.5 W=2 nf=1 ad='int((nf+1)/2) * W/nf * 0.29'
+ as='int((nf+2)/2) * W/nf * 0.29' pd='2*int((nf+1)/2) * (W/nf + 0.29)' ps='2*int((nf+2)/2) * (W/nf + 0.29)'
+ nrd='0.29 / W' nrs='0.29 / W' sa=0 sb=0 sd=0 mult=1 m=1
XM46 net24 enab_avdd avss avss sky130_fd_pr__nfet_g5v0d10v5 L=0.5 W=2 nf=1 ad='int((nf+1)/2) * W/nf * 0.29'
+ as='int((nf+2)/2) * W/nf * 0.29' pd='2*int((nf+1)/2) * (W/nf + 0.29)' ps='2*int((nf+2)/2) * (W/nf + 0.29)'
+ nrd='0.29 / W' nrs='0.29 / W' sa=0 sb=0 sd=0 mult=1 m=1
XM47 net25 enab_avdd avss avss sky130_fd_pr__nfet_g5v0d10v5 L=0.5 W=2 nf=1 ad='int((nf+1)/2) * W/nf * 0.29'
+ as='int((nf+2)/2) * W/nf * 0.29' pd='2*int((nf+1)/2) * (W/nf + 0.29)' ps='2*int((nf+2)/2) * (W/nf + 0.29)'
+ nrd='0.29 / W' nrs='0.29 / W' sa=0 sb=0 sd=0 mult=1 m=1
XM48 net28 enab_avdd avss avss sky130_fd_pr__nfet_g5v0d10v5 L=0.5 W=2 nf=1 ad='int((nf+1)/2) * W/nf * 0.29'
+ as='int((nf+2)/2) * W/nf * 0.29' pd='2*int((nf+1)/2) * (W/nf + 0.29)' ps='2*int((nf+2)/2) * (W/nf + 0.29)'
+ nrd='0.29 / W' nrs='0.29 / W' sa=0 sb=0 sd=0 mult=1 m=1
XM49 net29 enab_avdd avss avss sky130_fd_pr__nfet_g5v0d10v5 L=0.5 W=2 nf=1 ad='int((nf+1)/2) * W/nf * 0.29'
+ as='int((nf+2)/2) * W/nf * 0.29' pd='2*int((nf+1)/2) * (W/nf + 0.29)' ps='2*int((nf+2)/2) * (W/nf + 0.29)'
+ nrd='0.29 / W' nrs='0.29 / W' sa=0 sb=0 sd=0 mult=1 m=1
XM50 net23 ena_avdd avdd avdd sky130_fd_pr__pfet_g5v0d10v5 L=0.5 W=4 nf=1 ad='int((nf+1)/2) * W/nf * 0.29'
+ as='int((nf+2)/2) * W/nf * 0.29' pd='2*int((nf+1)/2) * (W/nf + 0.29)' ps='2*int((nf+2)/2) * (W/nf + 0.29)'
+ nrd='0.29 / W' nrs='0.29 / W' sa=0 sb=0 sd=0 mult=1 m=1
XM51 net26 ena_avdd avdd avdd sky130_fd_pr__pfet_g5v0d10v5 L=0.5 W=4 nf=1 ad='int((nf+1)/2) * W/nf * 0.29'
+ as='int((nf+2)/2) * W/nf * 0.29' pd='2*int((nf+1)/2) * (W/nf + 0.29)' ps='2*int((nf+2)/2) * (W/nf + 0.29)'
+ nrd='0.29 / W' nrs='0.29 / W' sa=0 sb=0 sd=0 mult=1 m=1
XM52 net27 ena_avdd avdd avdd sky130_fd_pr__pfet_g5v0d10v5 L=0.5 W=4 nf=1 ad='int((nf+1)/2) * W/nf * 0.29'
+ as='int((nf+2)/2) * W/nf * 0.29' pd='2*int((nf+1)/2) * (W/nf + 0.29)' ps='2*int((nf+2)/2) * (W/nf + 0.29)'
+ nrd='0.29 / W' nrs='0.29 / W' sa=0 sb=0 sd=0 mult=1 m=1
XM53 net30 ena_avdd avdd avdd sky130_fd_pr__pfet_g5v0d10v5 L=0.5 W=4 nf=1 ad='int((nf+1)/2) * W/nf * 0.29'
+ as='int((nf+2)/2) * W/nf * 0.29' pd='2*int((nf+1)/2) * (W/nf + 0.29)' ps='2*int((nf+2)/2) * (W/nf + 0.29)'
+ nrd='0.29 / W' nrs='0.29 / W' sa=0 sb=0 sd=0 mult=1 m=1
XM54 net45 ena dvss dvss sky130_fd_pr__nfet_01v8 L=0.15 W=1 nf=1 ad='int((nf+1)/2) * W/nf * 0.29' as='int((nf+2)/2) * W/nf * 0.29'
+ pd='2*int((nf+1)/2) * (W/nf + 0.29)' ps='2*int((nf+2)/2) * (W/nf + 0.29)' nrd='0.29 / W' nrs='0.29 / W'
+ sa=0 sb=0 sd=0 mult=1 m=1
XM55 net45 ena dvdd dvdd sky130_fd_pr__pfet_01v8 L=0.15 W=2 nf=1 ad='int((nf+1)/2) * W/nf * 0.29' as='int((nf+2)/2) * W/nf * 0.29'
+ pd='2*int((nf+1)/2) * (W/nf + 0.29)' ps='2*int((nf+2)/2) * (W/nf + 0.29)' nrd='0.29 / W' nrs='0.29 / W'
+ sa=0 sb=0 sd=0 mult=1 m=1
XM56 ena_avdd net44 avdd avdd sky130_fd_pr__pfet_g5v0d10v5 L=0.5 W=4 nf=1 ad='int((nf+1)/2) * W/nf * 0.29'
+ as='int((nf+2)/2) * W/nf * 0.29' pd='2*int((nf+1)/2) * (W/nf + 0.29)' ps='2*int((nf+2)/2) * (W/nf + 0.29)'
+ nrd='0.29 / W' nrs='0.29 / W' sa=0 sb=0 sd=0 mult=1 m=1
XM57 ena_avdd net44 avss avss sky130_fd_pr__nfet_g5v0d10v5 L=0.5 W=2 nf=1 ad='int((nf+1)/2) * W/nf * 0.29'
+ as='int((nf+2)/2) * W/nf * 0.29' pd='2*int((nf+1)/2) * (W/nf + 0.29)' ps='2*int((nf+2)/2) * (W/nf + 0.29)'
+ nrd='0.29 / W' nrs='0.29 / W' sa=0 sb=0 sd=0 mult=1 m=1
XM58 enab_avdd net43 avdd avdd sky130_fd_pr__pfet_g5v0d10v5 L=0.5 W=4 nf=1 ad='int((nf+1)/2) * W/nf * 0.29'
+ as='int((nf+2)/2) * W/nf * 0.29' pd='2*int((nf+1)/2) * (W/nf + 0.29)' ps='2*int((nf+2)/2) * (W/nf + 0.29)'
+ nrd='0.29 / W' nrs='0.29 / W' sa=0 sb=0 sd=0 mult=1 m=1
XM59 enab_avdd net43 avss avss sky130_fd_pr__nfet_g5v0d10v5 L=0.5 W=2 nf=1 ad='int((nf+1)/2) * W/nf * 0.29'
+ as='int((nf+2)/2) * W/nf * 0.29' pd='2*int((nf+1)/2) * (W/nf + 0.29)' ps='2*int((nf+2)/2) * (W/nf + 0.29)'
+ nrd='0.29 / W' nrs='0.29 / W' sa=0 sb=0 sd=0 mult=1 m=1
XM60 vb1 ena_avdd avdd avdd sky130_fd_pr__pfet_g5v0d10v5 L=0.5 W=4 nf=1 ad='int((nf+1)/2) * W/nf * 0.29'
+ as='int((nf+2)/2) * W/nf * 0.29' pd='2*int((nf+1)/2) * (W/nf + 0.29)' ps='2*int((nf+2)/2) * (W/nf + 0.29)'
+ nrd='0.29 / W' nrs='0.29 / W' sa=0 sb=0 sd=0 mult=1 m=1
XM61 net5 ena_avdd avdd avdd sky130_fd_pr__pfet_g5v0d10v5 L=0.5 W=4 nf=1 ad='int((nf+1)/2) * W/nf * 0.29'
+ as='int((nf+2)/2) * W/nf * 0.29' pd='2*int((nf+1)/2) * (W/nf + 0.29)' ps='2*int((nf+2)/2) * (W/nf + 0.29)'
+ nrd='0.29 / W' nrs='0.29 / W' sa=0 sb=0 sd=0 mult=1 m=1
XM62 vb4 enab_avdd avss avss sky130_fd_pr__nfet_g5v0d10v5 L=0.5 W=2 nf=1 ad='int((nf+1)/2) * W/nf * 0.29'
+ as='int((nf+2)/2) * W/nf * 0.29' pd='2*int((nf+1)/2) * (W/nf + 0.29)' ps='2*int((nf+2)/2) * (W/nf + 0.29)'
+ nrd='0.29 / W' nrs='0.29 / W' sa=0 sb=0 sd=0 mult=1 m=1
XM63 net6 enab_avdd avss avss sky130_fd_pr__nfet_g5v0d10v5 L=0.5 W=2 nf=1 ad='int((nf+1)/2) * W/nf * 0.29'
+ as='int((nf+2)/2) * W/nf * 0.29' pd='2*int((nf+1)/2) * (W/nf + 0.29)' ps='2*int((nf+2)/2) * (W/nf + 0.29)'
+ nrd='0.29 / W' nrs='0.29 / W' sa=0 sb=0 sd=0 mult=1 m=1
XM64 net2 enab_avdd avss avss sky130_fd_pr__nfet_g5v0d10v5 L=0.5 W=2 nf=1 ad='int((nf+1)/2) * W/nf * 0.29'
+ as='int((nf+2)/2) * W/nf * 0.29' pd='2*int((nf+1)/2) * (W/nf + 0.29)' ps='2*int((nf+2)/2) * (W/nf + 0.29)'
+ nrd='0.29 / W' nrs='0.29 / W' sa=0 sb=0 sd=0 mult=1 m=1
XM65 net3 ena_avdd avdd avdd sky130_fd_pr__pfet_g5v0d10v5 L=0.5 W=4 nf=1 ad='int((nf+1)/2) * W/nf * 0.29'
+ as='int((nf+2)/2) * W/nf * 0.29' pd='2*int((nf+1)/2) * (W/nf + 0.29)' ps='2*int((nf+2)/2) * (W/nf + 0.29)'
+ nrd='0.29 / W' nrs='0.29 / W' sa=0 sb=0 sd=0 mult=1 m=1
XM66 net4 ena_avdd avdd avdd sky130_fd_pr__pfet_g5v0d10v5 L=0.5 W=4 nf=1 ad='int((nf+1)/2) * W/nf * 0.29'
+ as='int((nf+2)/2) * W/nf * 0.29' pd='2*int((nf+1)/2) * (W/nf + 0.29)' ps='2*int((nf+2)/2) * (W/nf + 0.29)'
+ nrd='0.29 / W' nrs='0.29 / W' sa=0 sb=0 sd=0 mult=1 m=1
XM67 net31 enab_avdd avss avss sky130_fd_pr__nfet_g5v0d10v5 L=0.5 W=2 nf=1 ad='int((nf+1)/2) * W/nf * 0.29'
+ as='int((nf+2)/2) * W/nf * 0.29' pd='2*int((nf+1)/2) * (W/nf + 0.29)' ps='2*int((nf+2)/2) * (W/nf + 0.29)'
+ nrd='0.29 / W' nrs='0.29 / W' sa=0 sb=0 sd=0 mult=1 m=1
XM68 net22 ena_avdd avdd avdd sky130_fd_pr__pfet_g5v0d10v5 L=0.5 W=4 nf=1 ad='int((nf+1)/2) * W/nf * 0.29'
+ as='int((nf+2)/2) * W/nf * 0.29' pd='2*int((nf+1)/2) * (W/nf + 0.29)' ps='2*int((nf+2)/2) * (W/nf + 0.29)'
+ nrd='0.29 / W' nrs='0.29 / W' sa=0 sb=0 sd=0 mult=1 m=1
XM69 vb8 enab_avdd avss avss sky130_fd_pr__nfet_g5v0d10v5 L=0.5 W=2 nf=1 ad='int((nf+1)/2) * W/nf * 0.29'
+ as='int((nf+2)/2) * W/nf * 0.29' pd='2*int((nf+1)/2) * (W/nf + 0.29)' ps='2*int((nf+2)/2) * (W/nf + 0.29)'
+ nrd='0.29 / W' nrs='0.29 / W' sa=0 sb=0 sd=0 mult=1 m=1
XM70 vb5 ena_avdd avdd avdd sky130_fd_pr__pfet_g5v0d10v5 L=0.5 W=4 nf=1 ad='int((nf+1)/2) * W/nf * 0.29'
+ as='int((nf+2)/2) * W/nf * 0.29' pd='2*int((nf+1)/2) * (W/nf + 0.29)' ps='2*int((nf+2)/2) * (W/nf + 0.29)'
+ nrd='0.29 / W' nrs='0.29 / W' sa=0 sb=0 sd=0 mult=1 m=1
XM71 vb7 enab_avdd avss avss sky130_fd_pr__nfet_g5v0d10v5 L=0.5 W=2 nf=1 ad='int((nf+1)/2) * W/nf * 0.29'
+ as='int((nf+2)/2) * W/nf * 0.29' pd='2*int((nf+1)/2) * (W/nf + 0.29)' ps='2*int((nf+2)/2) * (W/nf + 0.29)'
+ nrd='0.29 / W' nrs='0.29 / W' sa=0 sb=0 sd=0 mult=1 m=1
XM72 vb6 ena_avdd avdd avdd sky130_fd_pr__pfet_g5v0d10v5 L=0.5 W=4 nf=1 ad='int((nf+1)/2) * W/nf * 0.29'
+ as='int((nf+2)/2) * W/nf * 0.29' pd='2*int((nf+1)/2) * (W/nf + 0.29)' ps='2*int((nf+2)/2) * (W/nf + 0.29)'
+ nrd='0.29 / W' nrs='0.29 / W' sa=0 sb=0 sd=0 mult=1 m=1
XM73 net10 enab_avdd avss avss sky130_fd_pr__nfet_g5v0d10v5 L=0.5 W=2 nf=1 ad='int((nf+1)/2) * W/nf * 0.29'
+ as='int((nf+2)/2) * W/nf * 0.29' pd='2*int((nf+1)/2) * (W/nf + 0.29)' ps='2*int((nf+2)/2) * (W/nf + 0.29)'
+ nrd='0.29 / W' nrs='0.29 / W' sa=0 sb=0 sd=0 mult=1 m=1
XM74 net9 ena_avdd avdd avdd sky130_fd_pr__pfet_g5v0d10v5 L=0.5 W=4 nf=1 ad='int((nf+1)/2) * W/nf * 0.29'
+ as='int((nf+2)/2) * W/nf * 0.29' pd='2*int((nf+1)/2) * (W/nf + 0.29)' ps='2*int((nf+2)/2) * (W/nf + 0.29)'
+ nrd='0.29 / W' nrs='0.29 / W' sa=0 sb=0 sd=0 mult=1 m=1
XM75 vb2 ena_avdd avdd avdd sky130_fd_pr__pfet_g5v0d10v5 L=0.5 W=4 nf=1 ad='int((nf+1)/2) * W/nf * 0.29'
+ as='int((nf+2)/2) * W/nf * 0.29' pd='2*int((nf+1)/2) * (W/nf + 0.29)' ps='2*int((nf+2)/2) * (W/nf + 0.29)'
+ nrd='0.29 / W' nrs='0.29 / W' sa=0 sb=0 sd=0 mult=1 m=1
XM76 vb3 enab_avdd avss avss sky130_fd_pr__nfet_g5v0d10v5 L=0.5 W=2 nf=1 ad='int((nf+1)/2) * W/nf * 0.29'
+ as='int((nf+2)/2) * W/nf * 0.29' pd='2*int((nf+1)/2) * (W/nf + 0.29)' ps='2*int((nf+2)/2) * (W/nf + 0.29)'
+ nrd='0.29 / W' nrs='0.29 / W' sa=0 sb=0 sd=0 mult=1 m=1
V_IB1 net21 net50 0
.save i(v_ib1)
V_IB2 net36 vb7 0
.save i(v_ib2)
V_IB3 vb2 net47 0
.save i(v_ib3)
V_IB4 vb6 net48 0
.save i(v_ib4)
V_IB5 net37 vb3 0
.save i(v_ib5)
V_IB6 net38 vb4 0
.save i(v_ib6)
V_IB7 vb1 net49 0
.save i(v_ib7)
XM77 vb7 enab_avdd avss avss sky130_fd_pr__nfet_g5v0d10v5 L=0.5 W=2 nf=1 ad='int((nf+1)/2) * W/nf * 0.29'
+ as='int((nf+2)/2) * W/nf * 0.29' pd='2*int((nf+1)/2) * (W/nf + 0.29)' ps='2*int((nf+2)/2) * (W/nf + 0.29)'
+ nrd='0.29 / W' nrs='0.29 / W' sa=0 sb=0 sd=0 mult=1 m=1
XM78 net32 enab_avdd net22 avdd sky130_fd_pr__pfet_g5v0d10v5 L=0.5 W=4 nf=1 ad='int((nf+1)/2) * W/nf * 0.29'
+ as='int((nf+2)/2) * W/nf * 0.29' pd='2*int((nf+1)/2) * (W/nf + 0.29)' ps='2*int((nf+2)/2) * (W/nf + 0.29)'
+ nrd='0.29 / W' nrs='0.29 / W' sa=0 sb=0 sd=0 mult=1 m=1
XM79 net32 ena_avdd avdd avdd sky130_fd_pr__pfet_g5v0d10v5 L=0.5 W=4 nf=1 ad='int((nf+1)/2) * W/nf * 0.29'
+ as='int((nf+2)/2) * W/nf * 0.29' pd='2*int((nf+1)/2) * (W/nf + 0.29)' ps='2*int((nf+2)/2) * (W/nf + 0.29)'
+ nrd='0.29 / W' nrs='0.29 / W' sa=0 sb=0 sd=0 mult=1 m=1
XM80 ibias ena_avdd net35 avss sky130_fd_pr__nfet_g5v0d10v5 L=0.5 W=2 nf=1 ad='int((nf+1)/2) * W/nf * 0.29'
+ as='int((nf+2)/2) * W/nf * 0.29' pd='2*int((nf+1)/2) * (W/nf + 0.29)' ps='2*int((nf+2)/2) * (W/nf + 0.29)'
+ nrd='0.29 / W' nrs='0.29 / W' sa=0 sb=0 sd=0 mult=1 m=1
XM81 net21 ena_avdd avdd avdd sky130_fd_pr__pfet_g5v0d10v5 L=0.5 W=4 nf=1 ad='int((nf+1)/2) * W/nf * 0.29'
+ as='int((nf+2)/2) * W/nf * 0.29' pd='2*int((nf+1)/2) * (W/nf + 0.29)' ps='2*int((nf+2)/2) * (W/nf + 0.29)'
+ nrd='0.29 / W' nrs='0.29 / W' sa=0 sb=0 sd=0 mult=1 m=1
XR1 vout net51 sky130_fd_pr__res_generic_po W=1 L=10 m=1
XR2 vout net52 sky130_fd_pr__res_generic_po W=1 L=1 m=1
**.ends
.end
